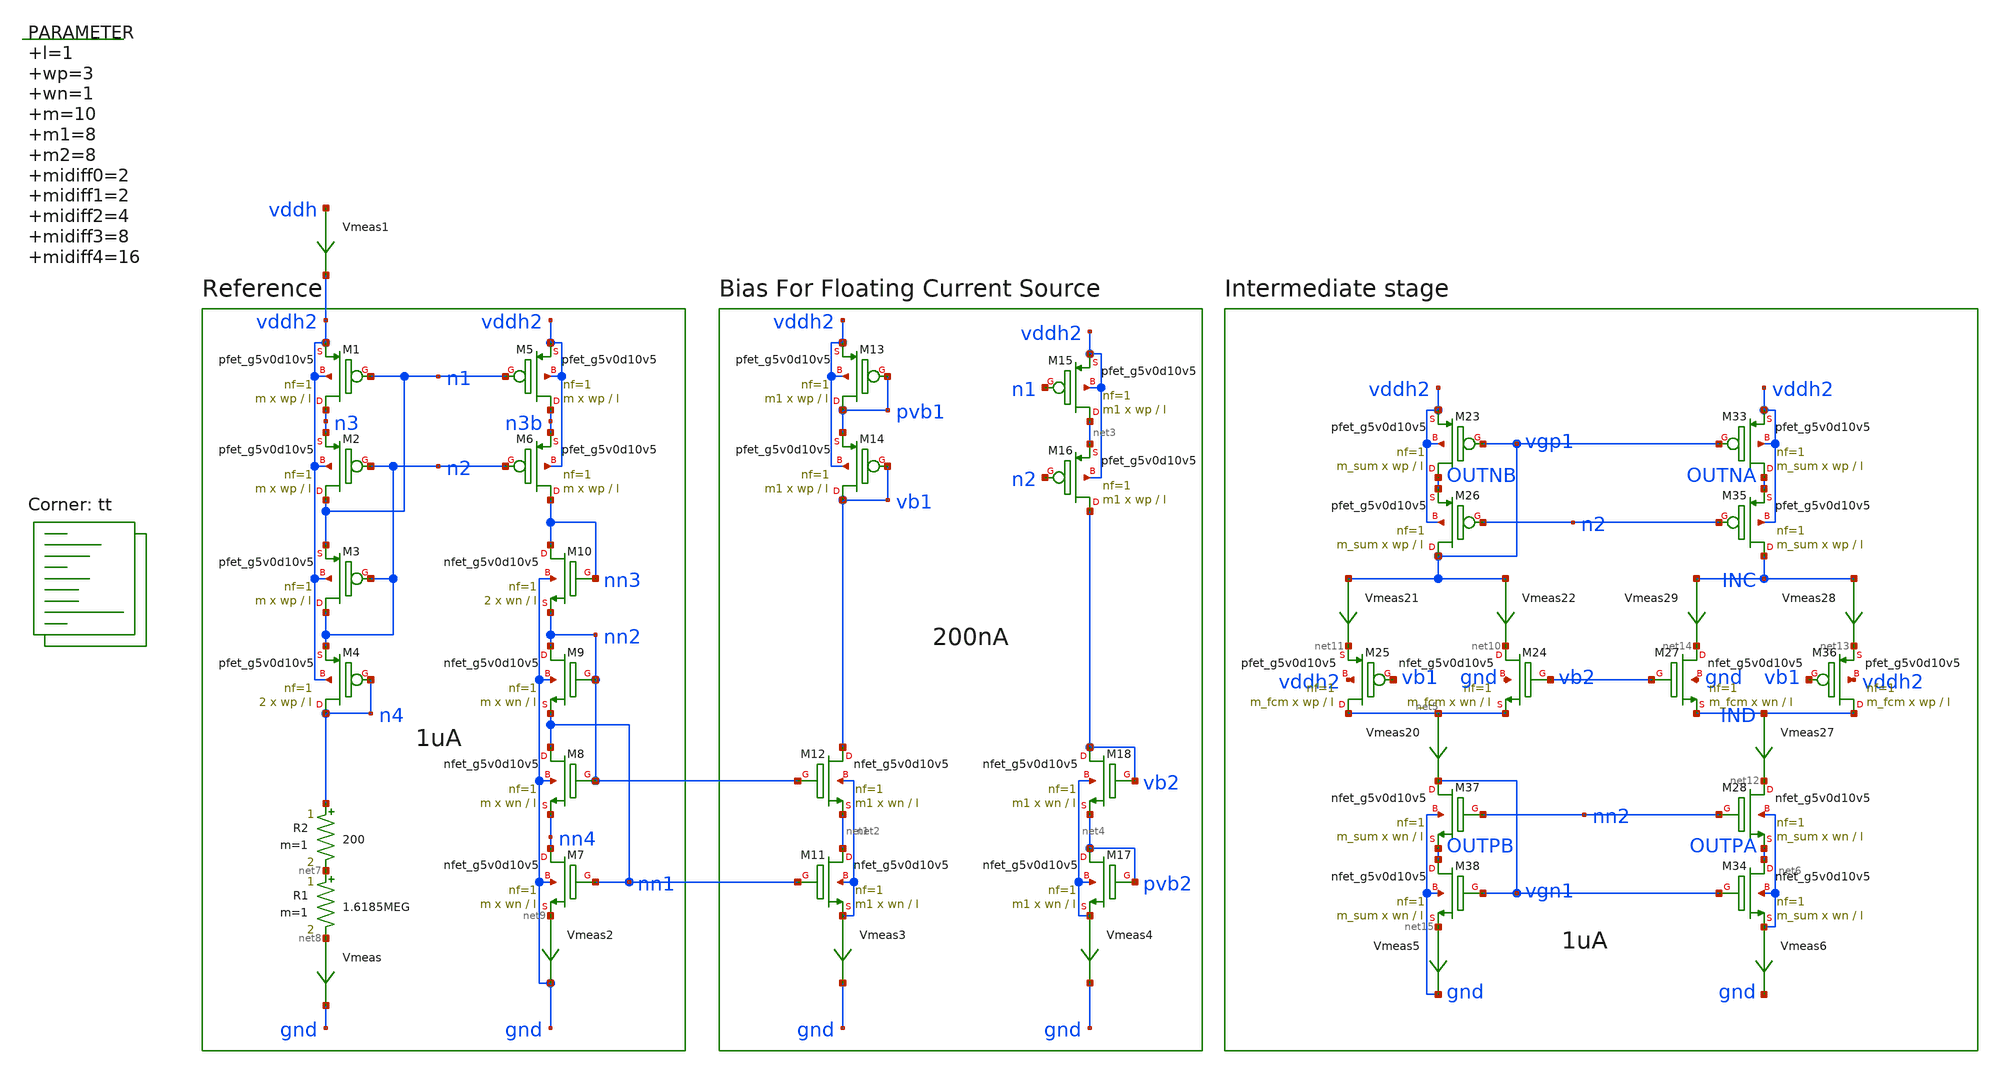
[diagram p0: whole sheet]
** sch_path: xschem/op_amp_biasing.sch
**.subckt op_amp_biasing
.param l=1 wp=3 wn=1 m=10 m1=8 m2=8 midiff0=2 midiff1=2 midiff2=4 midiff3=8 midiff4=16 m_sum=40
+ m_fcm=20
XM1 n3 n1 vddh2 vddh2 sky130_fd_pr__pfet_g5v0d10v5 L=l W=wp nf=1 ad='int((nf+1)/2) * W/nf * 0.29' as='int((nf+2)/2) * W/nf * 0.29'
+ pd='2*int((nf+1)/2) * (W/nf + 0.29)' ps='2*int((nf+2)/2) * (W/nf + 0.29)' nrd='0.29 / W' nrs='0.29 / W'
+ sa=0 sb=0 sd=0 mult=m m=m
R1 net7 net8 1.6185MEG m=1
Vmeas net8 gnd 0
.save i(vmeas)
R2 n4 net7 200 m=1
XM4 n4 n4 n2 vddh2 sky130_fd_pr__pfet_g5v0d10v5 L=l W=wp nf=1 ad='int((nf+1)/2) * W/nf * 0.29' as='int((nf+2)/2) * W/nf * 0.29'
+ pd='2*int((nf+1)/2) * (W/nf + 0.29)' ps='2*int((nf+2)/2) * (W/nf + 0.29)' nrd='0.29 / W' nrs='0.29 / W'
+ sa=0 sb=0 sd=0 mult=2 m=2
Vmeas1 vddh vddh2 0
.save i(vmeas1)
XM7 nn4 nn1 net9 gnd sky130_fd_pr__nfet_g5v0d10v5 L=l W=wn nf=1 ad='int((nf+1)/2) * W/nf * 0.29' as='int((nf+2)/2) * W/nf * 0.29'
+ pd='2*int((nf+1)/2) * (W/nf + 0.29)' ps='2*int((nf+2)/2) * (W/nf + 0.29)' nrd='0.29 / W' nrs='0.29 / W'
+ sa=0 sb=0 sd=0 mult=m m=m
XM8 nn1 nn2 nn4 gnd sky130_fd_pr__nfet_g5v0d10v5 L=l W=wn nf=1 ad='int((nf+1)/2) * W/nf * 0.29' as='int((nf+2)/2) * W/nf * 0.29'
+ pd='2*int((nf+1)/2) * (W/nf + 0.29)' ps='2*int((nf+2)/2) * (W/nf + 0.29)' nrd='0.29 / W' nrs='0.29 / W'
+ sa=0 sb=0 sd=0 mult=m m=m
XM9 nn2 nn2 nn1 gnd sky130_fd_pr__nfet_g5v0d10v5 L=l W=wn nf=1 ad='int((nf+1)/2) * W/nf * 0.29' as='int((nf+2)/2) * W/nf * 0.29'
+ pd='2*int((nf+1)/2) * (W/nf + 0.29)' ps='2*int((nf+2)/2) * (W/nf + 0.29)' nrd='0.29 / W' nrs='0.29 / W'
+ sa=0 sb=0 sd=0 mult=m m=m
XM10 nn3 nn3 nn2 gnd sky130_fd_pr__nfet_g5v0d10v5 L=l W=wn nf=1 ad='int((nf+1)/2) * W/nf * 0.29' as='int((nf+2)/2) * W/nf * 0.29'
+ pd='2*int((nf+1)/2) * (W/nf + 0.29)' ps='2*int((nf+2)/2) * (W/nf + 0.29)' nrd='0.29 / W' nrs='0.29 / W'
+ sa=0 sb=0 sd=0 mult=2 m=2
Vmeas2 net9 gnd 0
.save i(vmeas2)
XM11 net1 nn1 net2 net2 sky130_fd_pr__nfet_g5v0d10v5 L=l W=wn nf=1 ad='int((nf+1)/2) * W/nf * 0.29' as='int((nf+2)/2) * W/nf * 0.29'
+ pd='2*int((nf+1)/2) * (W/nf + 0.29)' ps='2*int((nf+2)/2) * (W/nf + 0.29)' nrd='0.29 / W' nrs='0.29 / W'
+ sa=0 sb=0 sd=0 mult=m1 m=m1
XM12 vb1 nn2 net1 net2 sky130_fd_pr__nfet_g5v0d10v5 L=l W=wn nf=1 ad='int((nf+1)/2) * W/nf * 0.29' as='int((nf+2)/2) * W/nf * 0.29'
+ pd='2*int((nf+1)/2) * (W/nf + 0.29)' ps='2*int((nf+2)/2) * (W/nf + 0.29)' nrd='0.29 / W' nrs='0.29 / W'
+ sa=0 sb=0 sd=0 mult=m1 m=m1
Vmeas3 net2 gnd 0
.save i(vmeas3)
XM17 pvb2 pvb2 net4 net4 sky130_fd_pr__nfet_g5v0d10v5 L=l W=wn nf=1 ad='int((nf+1)/2) * W/nf * 0.29'
+ as='int((nf+2)/2) * W/nf * 0.29' pd='2*int((nf+1)/2) * (W/nf + 0.29)' ps='2*int((nf+2)/2) * (W/nf + 0.29)'
+ nrd='0.29 / W' nrs='0.29 / W' sa=0 sb=0 sd=0 mult=m1 m=m1
XM18 vb2 vb2 pvb2 net4 sky130_fd_pr__nfet_g5v0d10v5 L=l W=wn nf=1 ad='int((nf+1)/2) * W/nf * 0.29' as='int((nf+2)/2) * W/nf * 0.29'
+ pd='2*int((nf+1)/2) * (W/nf + 0.29)' ps='2*int((nf+2)/2) * (W/nf + 0.29)' nrd='0.29 / W' nrs='0.29 / W'
+ sa=0 sb=0 sd=0 mult=m1 m=m1
Vmeas4 net4 gnd 0
.save i(vmeas4)
Vmeas20 net5 vgn1 0
.save i(vmeas20)
XM23 OUTNB vgp1 vddh2 vddh2 sky130_fd_pr__pfet_g5v0d10v5 L=l W=wp nf=1 ad='int((nf+1)/2) * W/nf * 0.29'
+ as='int((nf+2)/2) * W/nf * 0.29' pd='2*int((nf+1)/2) * (W/nf + 0.29)' ps='2*int((nf+2)/2) * (W/nf + 0.29)'
+ nrd='0.29 / W' nrs='0.29 / W' sa=0 sb=0 sd=0 mult=m_sum m=m_sum
XM24 net10 vb2 net5 gnd sky130_fd_pr__nfet_g5v0d10v5 L=l W=wn nf=1 ad='int((nf+1)/2) * W/nf * 0.29' as='int((nf+2)/2) * W/nf * 0.29'
+ pd='2*int((nf+1)/2) * (W/nf + 0.29)' ps='2*int((nf+2)/2) * (W/nf + 0.29)' nrd='0.29 / W' nrs='0.29 / W'
+ sa=0 sb=0 sd=0 mult=m_fcm m=m_fcm
Vmeas21 vgp1 net11 0
.save i(vmeas21)
Vmeas22 vgp1 net10 0
.save i(vmeas22)
XM25 net5 vb1 net11 vddh2 sky130_fd_pr__pfet_g5v0d10v5 L=l W=wp nf=1 ad='int((nf+1)/2) * W/nf * 0.29'
+ as='int((nf+2)/2) * W/nf * 0.29' pd='2*int((nf+1)/2) * (W/nf + 0.29)' ps='2*int((nf+2)/2) * (W/nf + 0.29)'
+ nrd='0.29 / W' nrs='0.29 / W' sa=0 sb=0 sd=0 mult=m_fcm m=m_fcm
Vmeas27 IND net12 0
.save i(vmeas27)
Vmeas28 INC net13 0
.save i(vmeas28)
Vmeas29 INC net14 0
.save i(vmeas29)
XM26 vgp1 n2 OUTNB vddh2 sky130_fd_pr__pfet_g5v0d10v5 L=l W=wp nf=1 ad='int((nf+1)/2) * W/nf * 0.29'
+ as='int((nf+2)/2) * W/nf * 0.29' pd='2*int((nf+1)/2) * (W/nf + 0.29)' ps='2*int((nf+2)/2) * (W/nf + 0.29)'
+ nrd='0.29 / W' nrs='0.29 / W' sa=0 sb=0 sd=0 mult=m_sum m=m_sum
XM33 OUTNA vgp1 vddh2 vddh2 sky130_fd_pr__pfet_g5v0d10v5 L=l W=wp nf=1 ad='int((nf+1)/2) * W/nf * 0.29'
+ as='int((nf+2)/2) * W/nf * 0.29' pd='2*int((nf+1)/2) * (W/nf + 0.29)' ps='2*int((nf+2)/2) * (W/nf + 0.29)'
+ nrd='0.29 / W' nrs='0.29 / W' sa=0 sb=0 sd=0 mult=m_sum m=m_sum
XM35 INC n2 OUTNA vddh2 sky130_fd_pr__pfet_g5v0d10v5 L=l W=wp nf=1 ad='int((nf+1)/2) * W/nf * 0.29' as='int((nf+2)/2) * W/nf * 0.29'
+ pd='2*int((nf+1)/2) * (W/nf + 0.29)' ps='2*int((nf+2)/2) * (W/nf + 0.29)' nrd='0.29 / W' nrs='0.29 / W'
+ sa=0 sb=0 sd=0 mult=m_sum m=m_sum
XM28 net12 nn2 OUTPA net6 sky130_fd_pr__nfet_g5v0d10v5 L=l W=wn nf=1 ad='int((nf+1)/2) * W/nf * 0.29'
+ as='int((nf+2)/2) * W/nf * 0.29' pd='2*int((nf+1)/2) * (W/nf + 0.29)' ps='2*int((nf+2)/2) * (W/nf + 0.29)'
+ nrd='0.29 / W' nrs='0.29 / W' sa=0 sb=0 sd=0 mult=m_sum m=m_sum
XM34 OUTPA vgn1 net6 net6 sky130_fd_pr__nfet_g5v0d10v5 L=l W=wn nf=1 ad='int((nf+1)/2) * W/nf * 0.29'
+ as='int((nf+2)/2) * W/nf * 0.29' pd='2*int((nf+1)/2) * (W/nf + 0.29)' ps='2*int((nf+2)/2) * (W/nf + 0.29)'
+ nrd='0.29 / W' nrs='0.29 / W' sa=0 sb=0 sd=0 mult=m_sum m=m_sum
XM37 vgn1 nn2 OUTPB gnd sky130_fd_pr__nfet_g5v0d10v5 L=l W=wn nf=1 ad='int((nf+1)/2) * W/nf * 0.29' as='int((nf+2)/2) * W/nf * 0.29'
+ pd='2*int((nf+1)/2) * (W/nf + 0.29)' ps='2*int((nf+2)/2) * (W/nf + 0.29)' nrd='0.29 / W' nrs='0.29 / W'
+ sa=0 sb=0 sd=0 mult=m_sum m=m_sum
XM38 OUTPB vgn1 net15 gnd sky130_fd_pr__nfet_g5v0d10v5 L=l W=wn nf=1 ad='int((nf+1)/2) * W/nf * 0.29'
+ as='int((nf+2)/2) * W/nf * 0.29' pd='2*int((nf+1)/2) * (W/nf + 0.29)' ps='2*int((nf+2)/2) * (W/nf + 0.29)'
+ nrd='0.29 / W' nrs='0.29 / W' sa=0 sb=0 sd=0 mult=m_sum m=m_sum
XM36 IND vb1 net13 vddh2 sky130_fd_pr__pfet_g5v0d10v5 L=l W=wp nf=1 ad='int((nf+1)/2) * W/nf * 0.29'
+ as='int((nf+2)/2) * W/nf * 0.29' pd='2*int((nf+1)/2) * (W/nf + 0.29)' ps='2*int((nf+2)/2) * (W/nf + 0.29)'
+ nrd='0.29 / W' nrs='0.29 / W' sa=0 sb=0 sd=0 mult=m_fcm m=m_fcm
XM27 net14 vb2 IND gnd sky130_fd_pr__nfet_g5v0d10v5 L=l W=wn nf=1 ad='int((nf+1)/2) * W/nf * 0.29' as='int((nf+2)/2) * W/nf * 0.29'
+ pd='2*int((nf+1)/2) * (W/nf + 0.29)' ps='2*int((nf+2)/2) * (W/nf + 0.29)' nrd='0.29 / W' nrs='0.29 / W'
+ sa=0 sb=0 sd=0 mult=m_fcm m=m_fcm
XM2 n1 n2 n3 vddh2 sky130_fd_pr__pfet_g5v0d10v5 L=l W=wp nf=1 ad='int((nf+1)/2) * W/nf * 0.29' as='int((nf+2)/2) * W/nf * 0.29'
+ pd='2*int((nf+1)/2) * (W/nf + 0.29)' ps='2*int((nf+2)/2) * (W/nf + 0.29)' nrd='0.29 / W' nrs='0.29 / W'
+ sa=0 sb=0 sd=0 mult=m m=m
XM3 n2 n2 n1 vddh2 sky130_fd_pr__pfet_g5v0d10v5 L=l W=wp nf=1 ad='int((nf+1)/2) * W/nf * 0.29' as='int((nf+2)/2) * W/nf * 0.29'
+ pd='2*int((nf+1)/2) * (W/nf + 0.29)' ps='2*int((nf+2)/2) * (W/nf + 0.29)' nrd='0.29 / W' nrs='0.29 / W'
+ sa=0 sb=0 sd=0 mult=m m=m
XM5 n3b n1 vddh2 vddh2 sky130_fd_pr__pfet_g5v0d10v5 L=l W=wp nf=1 ad='int((nf+1)/2) * W/nf * 0.29' as='int((nf+2)/2) * W/nf * 0.29'
+ pd='2*int((nf+1)/2) * (W/nf + 0.29)' ps='2*int((nf+2)/2) * (W/nf + 0.29)' nrd='0.29 / W' nrs='0.29 / W'
+ sa=0 sb=0 sd=0 mult=m m=m
XM6 nn3 n2 n3b vddh2 sky130_fd_pr__pfet_g5v0d10v5 L=l W=wp nf=1 ad='int((nf+1)/2) * W/nf * 0.29' as='int((nf+2)/2) * W/nf * 0.29'
+ pd='2*int((nf+1)/2) * (W/nf + 0.29)' ps='2*int((nf+2)/2) * (W/nf + 0.29)' nrd='0.29 / W' nrs='0.29 / W'
+ sa=0 sb=0 sd=0 mult=m m=m
XM13 pvb1 pvb1 vddh2 vddh2 sky130_fd_pr__pfet_g5v0d10v5 L=l W=wp nf=1 ad='int((nf+1)/2) * W/nf * 0.29'
+ as='int((nf+2)/2) * W/nf * 0.29' pd='2*int((nf+1)/2) * (W/nf + 0.29)' ps='2*int((nf+2)/2) * (W/nf + 0.29)'
+ nrd='0.29 / W' nrs='0.29 / W' sa=0 sb=0 sd=0 mult=m1 m=m1
XM14 vb1 vb1 pvb1 vddh2 sky130_fd_pr__pfet_g5v0d10v5 L=l W=wp nf=1 ad='int((nf+1)/2) * W/nf * 0.29' as='int((nf+2)/2) * W/nf * 0.29'
+ pd='2*int((nf+1)/2) * (W/nf + 0.29)' ps='2*int((nf+2)/2) * (W/nf + 0.29)' nrd='0.29 / W' nrs='0.29 / W'
+ sa=0 sb=0 sd=0 mult=m1 m=m1
XM15 net3 n1 vddh2 vddh2 sky130_fd_pr__pfet_g5v0d10v5 L=l W=wp nf=1 ad='int((nf+1)/2) * W/nf * 0.29'
+ as='int((nf+2)/2) * W/nf * 0.29' pd='2*int((nf+1)/2) * (W/nf + 0.29)' ps='2*int((nf+2)/2) * (W/nf + 0.29)'
+ nrd='0.29 / W' nrs='0.29 / W' sa=0 sb=0 sd=0 mult=m1 m=m1
XM16 vb2 n2 net3 vddh2 sky130_fd_pr__pfet_g5v0d10v5 L=l W=wp nf=1 ad='int((nf+1)/2) * W/nf * 0.29' as='int((nf+2)/2) * W/nf * 0.29'
+ pd='2*int((nf+1)/2) * (W/nf + 0.29)' ps='2*int((nf+2)/2) * (W/nf + 0.29)' nrd='0.29 / W' nrs='0.29 / W'
+ sa=0 sb=0 sd=0 mult=m1 m=m1
Vmeas5 net15 gnd 0
.save i(vmeas5)
Vmeas6 net6 gnd 0
.save i(vmeas6)
**** begin user architecture code
.lib $::SKYWATER_MODELS/sky130.lib.spice tt



  .option wnflag=1
  .option safecurrents
  ********************Static Current Sources***************************
  .param iref=10u
  ********************Static Voltage Sources***************************
  Vddh vddh gnd dc 5.5
  ********************Simulation Commands*****************************
  .control
     reset
     save all
     dc R1 1.9meg 2.2meg 10
     write biasing-tb.raw
     set appendwrite
*    quit 0
  .endc



**** end user architecture code
**.ends
.end
